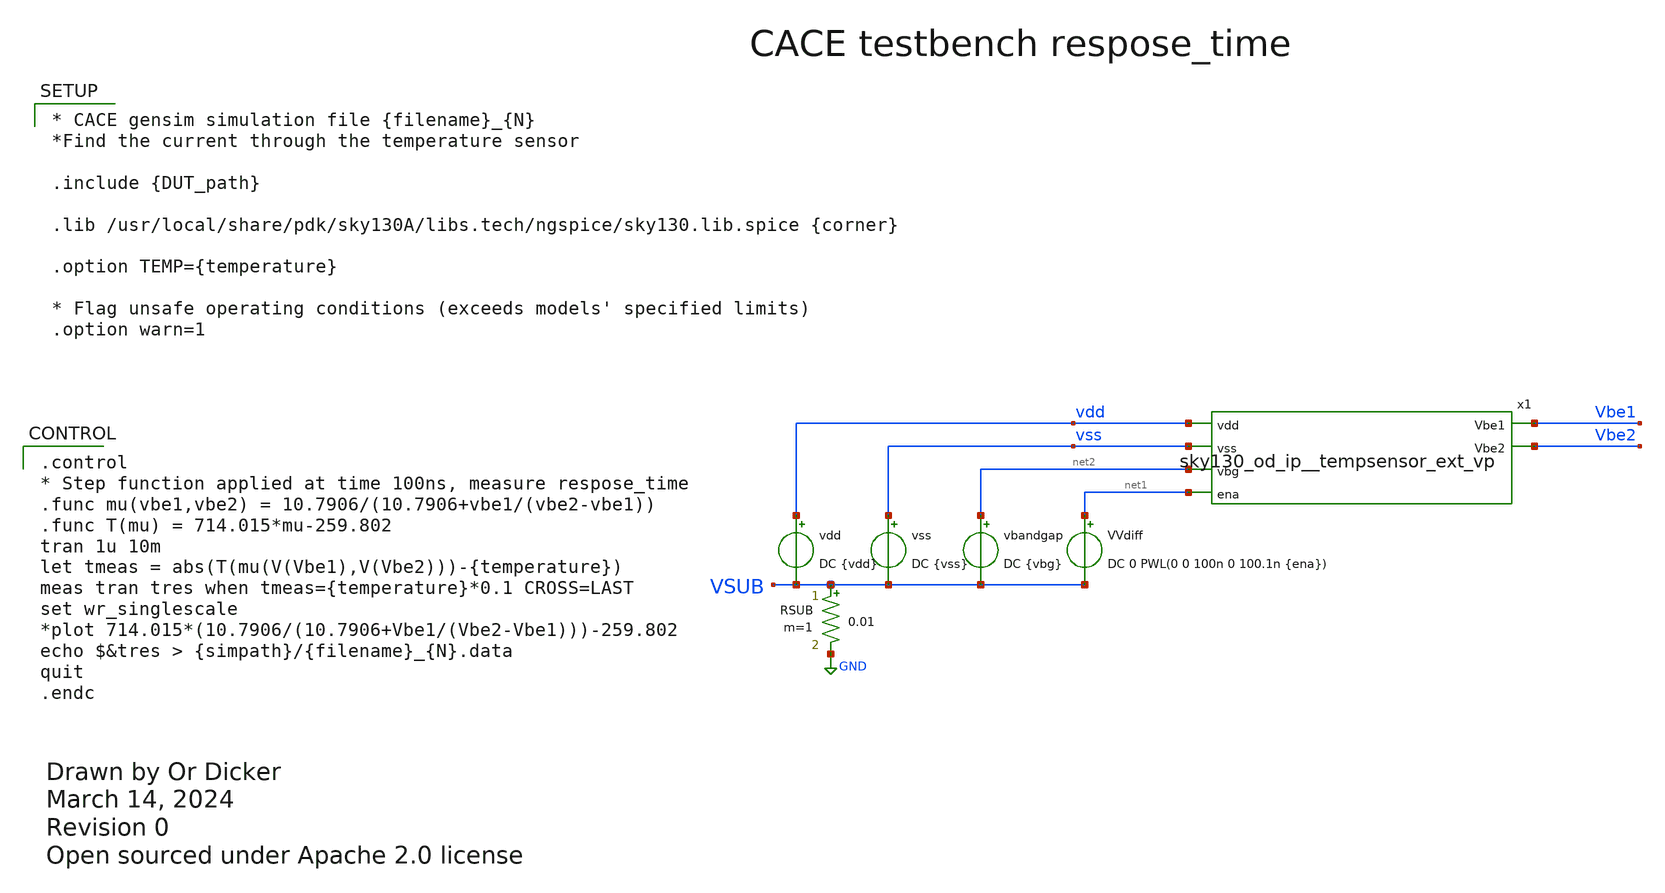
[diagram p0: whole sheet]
** sch_path: cace/templates/respose_time.sch
* Open sourced under Apache 2.0 license
**.subckt respose_time
vss vss VSUB DC {vss}
vdd vdd VSUB DC {vdd}
RSUB VSUB GND 0.01 m=1
VVdiff net1 VSUB DC 0 PWL(0 0 100n 0 100.1n {ena})
x1 vdd vss net2 Vbe1 Vbe2 net1 sky130_od_ip__tempsensor_ext_vp
vbandgap net2 VSUB DC {vbg}
**** begin user architecture code

.control
* Step function applied at time 100ns, measure respose_time
.func mu(vbe1,vbe2) = 10.7906/(10.7906+vbe1/(vbe2-vbe1))
.func T(mu) = 714.015*mu-259.802
tran 1u 10m
let tmeas = abs(T(mu(V(Vbe1),V(Vbe2)))-{temperature})
meas tran tres when tmeas={temperature}*0.1 CROSS=LAST
set wr_singlescale
*plot 714.015*(10.7906/(10.7906+Vbe1/(Vbe2-Vbe1)))-259.802
echo $&tres > {simpath}/{filename}_{N}.data
quit
.endc



* CACE gensim simulation file {filename}_{N}
*Find the current through the temperature sensor

.include {DUT_path}

.lib /usr/local/share/pdk/sky130A/libs.tech/ngspice/sky130.lib.spice {corner}

.option TEMP={temperature}

* Flag unsafe operating conditions (exceeds models' specified limits)
.option warn=1


**** end user architecture code
**.ends
.GLOBAL GND
.end
